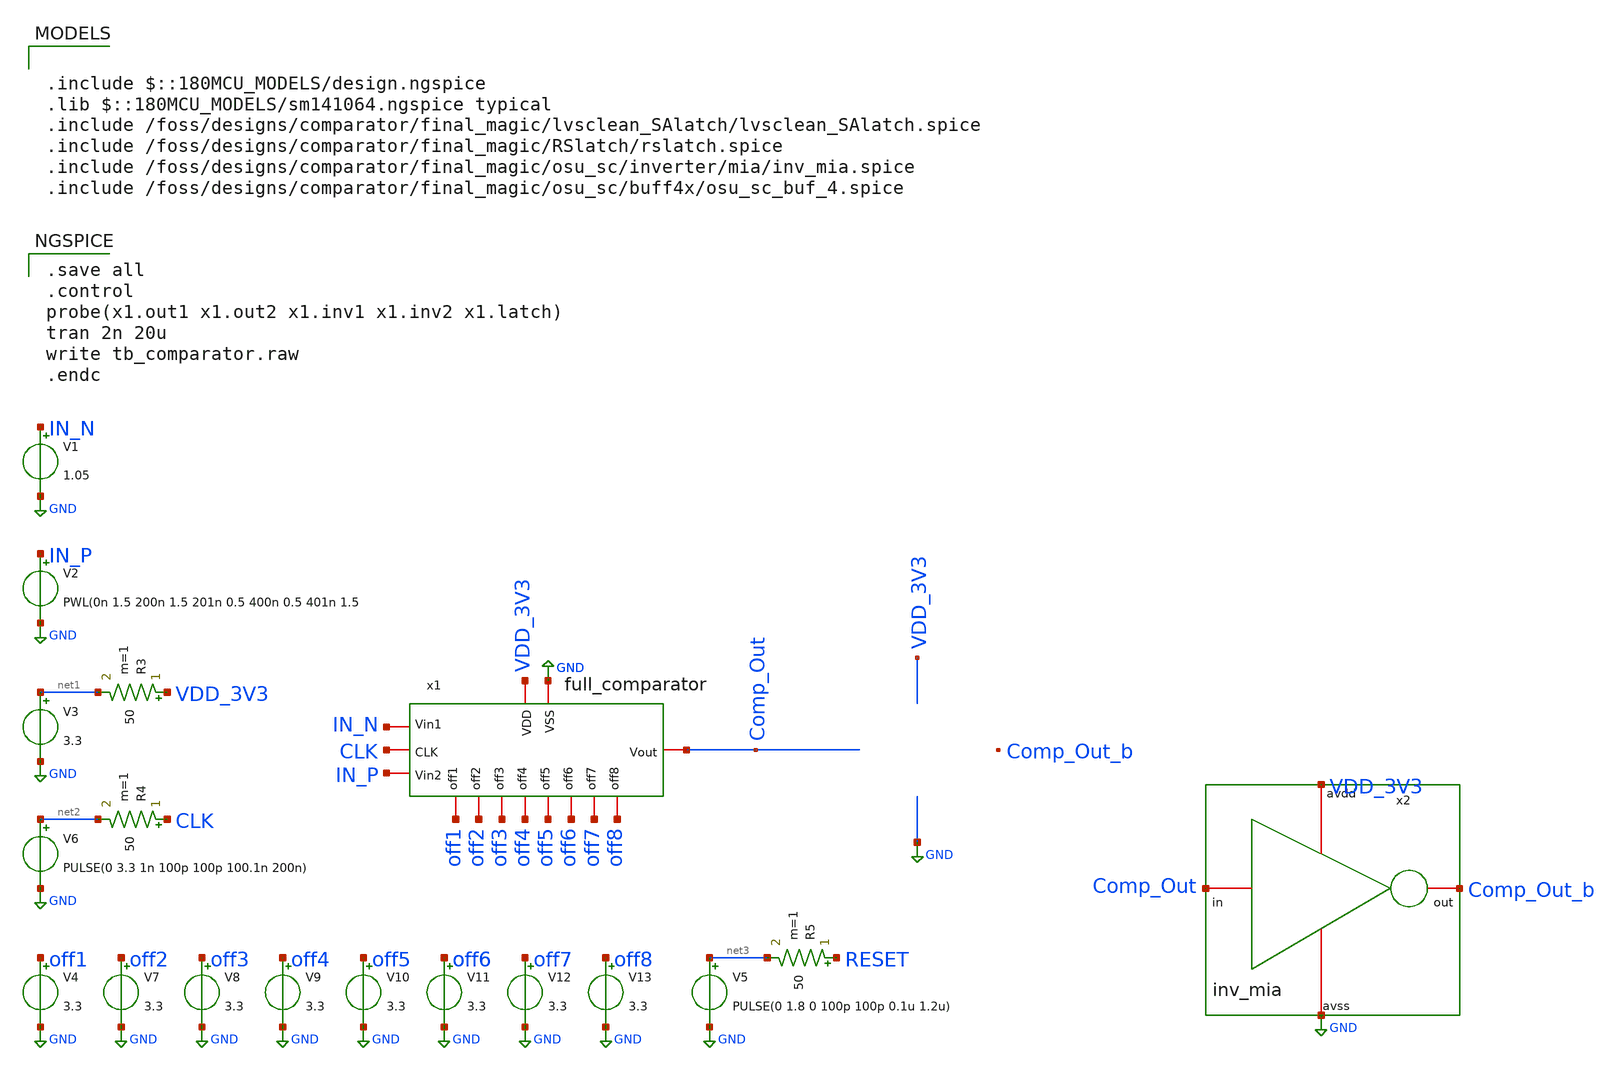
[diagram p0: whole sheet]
** sch_path: designs/comparator/final_magic/tb_comparator.sch
**.subckt tb_comparator
x1 off1 VDD_3V3 GND off2 CLK off3 IN_N off4 IN_P off5 Comp_Out off6 off7 off8 full_comparator
V4 off1 GND 3.3
V7 off2 GND 3.3
V8 off3 GND 3.3
V9 off4 GND 3.3
V10 off5 GND 3.3
V11 off6 GND 3.3
V12 off7 GND 3.3
V13 off8 GND 3.3
V3 net1 GND 3.3
V6 net2 GND PULSE(0 3.3 1n 100p 100p 100.1n 200n)
R3 VDD_3V3 net1 50 m=1
R4 CLK net2 50 m=1
V2 IN_P GND PWL(0n 1.5 200n 1.5 201n 0.5 400n 0.5 401n 1.5
V1 IN_N GND 1.05
V5 net3 GND PULSE(0 1.8 0 100p 100p 0.1u 1.2u)
R5 RESET net3 50 m=1
x2 VDD_3V3 Comp_Out Comp_Out_b GND inv_mia
**** begin user architecture code

.include $::180MCU_MODELS/design.ngspice
.lib $::180MCU_MODELS/sm141064.ngspice typical
.include /foss/designs/comparator/final_magic/lvsclean_SAlatch/lvsclean_SAlatch.spice
.include /foss/designs/comparator/final_magic/RSlatch/rslatch.spice
.include /foss/designs/comparator/final_magic/osu_sc/inverter/mia/inv_mia.spice
.include /foss/designs/comparator/final_magic/osu_sc/buff4x/osu_sc_buf_4.spice


.save all
.control
probe(x1.out1 x1.out2 x1.inv1 x1.inv2 x1.latch)
tran 2n 20u
write tb_comparator.raw
.endc

**** end user architecture code
**.ends
.GLOBAL GND
.end
